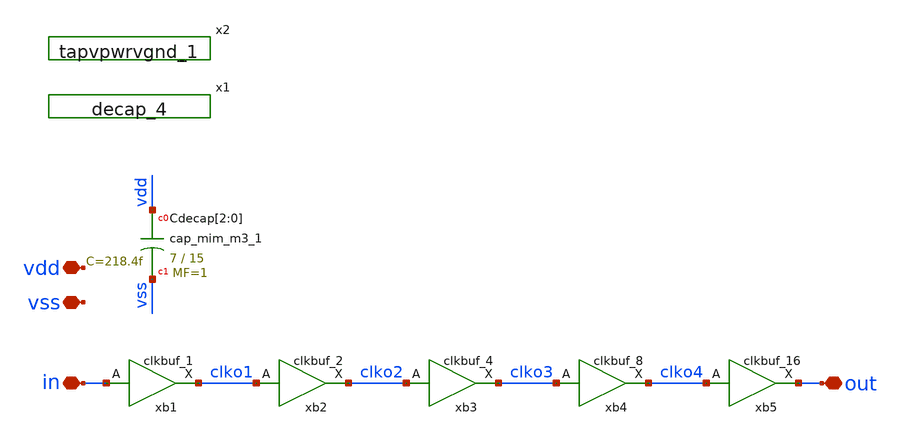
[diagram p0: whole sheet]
** sch_path: xschem/support/clkbuf.sch
**.subckt clkbuf vss vdd in out
*.iopin vss
*.iopin vdd
*.iopin in
*.iopin out
xb1 in vss vss vdd vdd clko1 sky130_fd_sc_hd__clkbuf_1
xb2 clko1 vss vss vdd vdd clko2 sky130_fd_sc_hd__clkbuf_2
xb3 clko2 vss vss vdd vdd clko3 sky130_fd_sc_hd__clkbuf_4
xb4 clko3 vss vss vdd vdd clko4 sky130_fd_sc_hd__clkbuf_8
xb5 clko4 vss vss vdd vdd out sky130_fd_sc_hd__clkbuf_16
x1 vss vss vdd vdd sky130_fd_sc_hd__decap_4
x2 vss vdd sky130_fd_sc_hd__tapvpwrvgnd_1
XCdecap[2] vdd vss sky130_fd_pr__cap_mim_m3_1 W=7 L=15 MF=1 m=1
XCdecap[1] vdd vss sky130_fd_pr__cap_mim_m3_1 W=7 L=15 MF=1 m=1
XCdecap[0] vdd vss sky130_fd_pr__cap_mim_m3_1 W=7 L=15 MF=1 m=1
**.ends
.end
